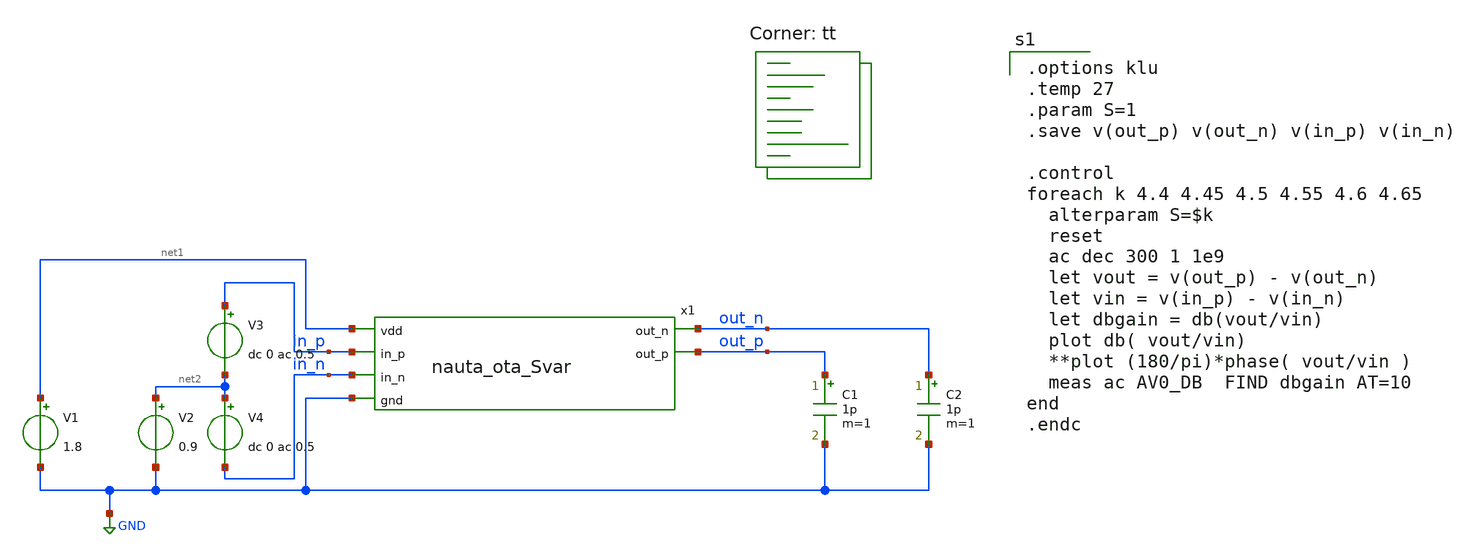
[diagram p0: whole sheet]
** sch_path: xsch/nauta_ota_Svar_tb.sch
**.subckt nauta_ota_Svar_tb
V1 net1 GND 1.8
V2 net2 GND 0.9
V3 in_p net2 dc 0 ac 0.5
V4 net2 in_n dc 0 ac 0.5
C1 out_p GND 1p m=1
C2 out_n GND 1p m=1
x1 net1 out_n in_p out_p in_n GND nauta_ota_Svar
**** begin user architecture code
.lib $::SKYWATER_MODELS/sky130.lib.spice tt

.options klu
.temp 27
.param S=1
.save v(out_p) v(out_n) v(in_p) v(in_n)

.control
foreach k 4.4 4.45 4.5 4.55 4.6 4.65
  alterparam S=$k
  reset
  ac dec 300 1 1e9
  let vout = v(out_p) - v(out_n)
  let vin = v(in_p) - v(in_n)
  let dbgain = db(vout/vin)
  plot db( vout/vin)
  **plot (180/pi)*phase( vout/vin )
  meas ac AV0_DB  FIND dbgain AT=10
end
.endc



**** end user architecture code
**.ends
.GLOBAL GND
.end
